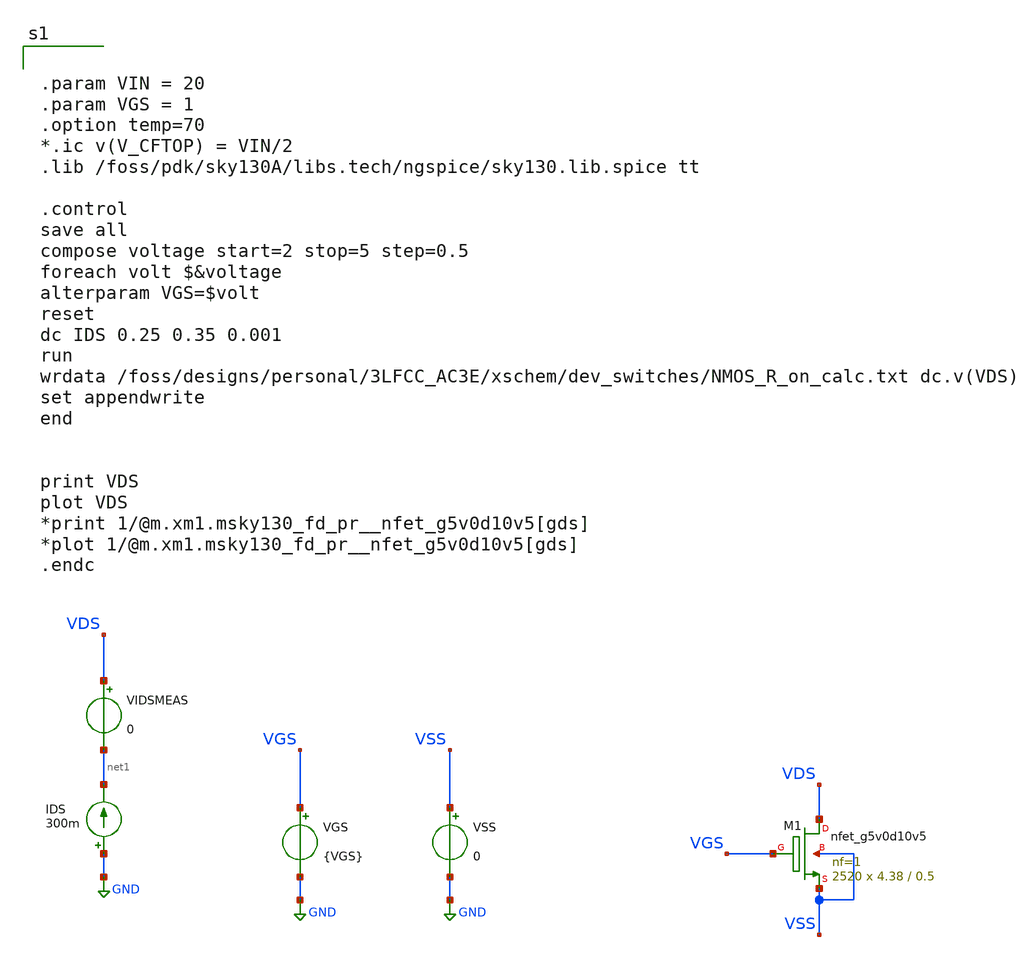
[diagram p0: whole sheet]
** sch_path: Notebooks/3LFCC/NMOS_allfingers_RONcalc_v2p2_vicente.sch
**.subckt NMOS_allfingers_RONcalc_v2p2_vicente
XM1 VDS VGS VSS VSS sky130_fd_pr__nfet_g5v0d10v5 L=0.5 W=4.38 nf=1 ad='int((nf+1)/2) * W/nf * 0.29' as='int((nf+2)/2) * W/nf * 0.29'
+ pd='2*int((nf+1)/2) * (W/nf + 0.29)' ps='2*int((nf+2)/2) * (W/nf + 0.29)' nrd='0.29 / W' nrs='0.29 / W'
+ sa=0 sb=0 sd=0 mult=2520 m=2520
VGS VGS GND {VGS}
VSS VSS GND 0
IDS GND net1 300m
VIDSMEAS VDS net1 0
**** begin user architecture code


.param VIN = 20
.param VGS = 1
.option temp=70
*.ic v(V_CFTOP) = VIN/2
.lib /foss/pdk/sky130A/libs.tech/ngspice/sky130.lib.spice tt

.control
save all
compose voltage start=2 stop=5 step=0.5
foreach volt $&voltage
alterparam VGS=$volt
reset
dc IDS 0.25 0.35 0.001
run
wrdata /foss/designs/personal/3LFCC_AC3E/xschem/dev_switches/NMOS_R_on_calc.txt dc.v(VDS)
set appendwrite
end


print VDS
plot VDS
*print 1/@m.xm1.msky130_fd_pr__nfet_g5v0d10v5[gds]
*plot 1/@m.xm1.msky130_fd_pr__nfet_g5v0d10v5[gds]
.endc



**** end user architecture code
**.ends
.GLOBAL GND
.end
